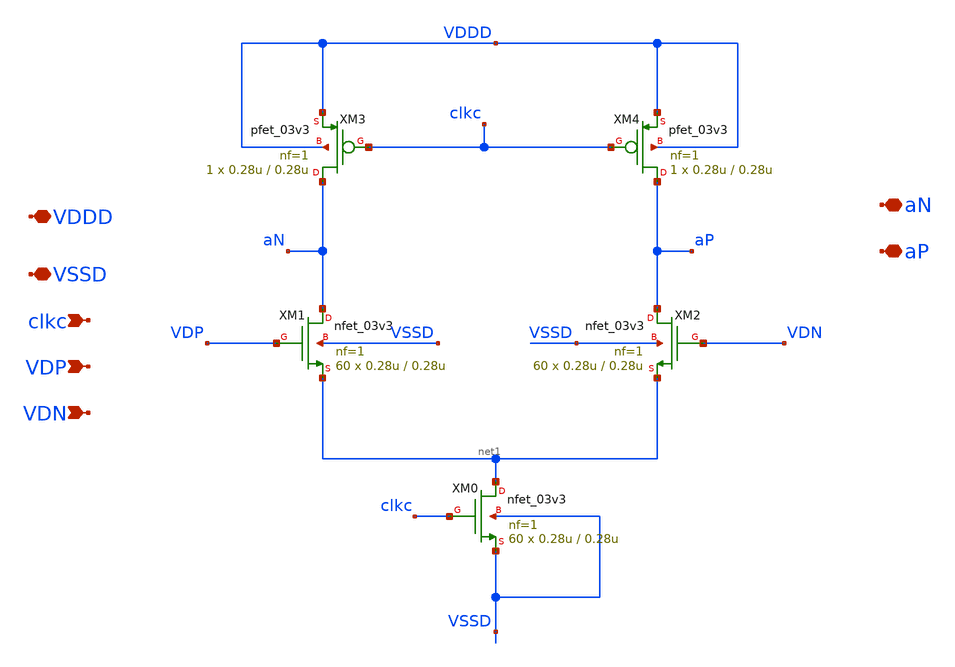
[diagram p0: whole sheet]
** sch_path: SAR_ADC/blocks/Dynamic_Comparator/Dynamic_Comparator_opamp.sch
**.subckt Dynamic_Comparator_opamp VDDD VSSD clkc VDP VDN aN aP
*.iopin VDDD
*.iopin VSSD
*.ipin clkc
*.ipin VDP
*.ipin VDN
*.iopin aN
*.iopin aP
XM0 net1 clkc VSSD VSSD nfet_03v3 L=0.28u W=0.28u nf=1 ad='int((nf+1)/2) * W/nf * 0.18u' as='int((nf+2)/2) * W/nf * 0.18u'
+ pd='2*int((nf+1)/2) * (W/nf + 0.18u)' ps='2*int((nf+2)/2) * (W/nf + 0.18u)' nrd='0.18u / W' nrs='0.18u / W'
+ sa=0 sb=0 sd=0 m=60
XM1 aN VDP net1 VSSD nfet_03v3 L=0.28u W=0.28u nf=1 ad='int((nf+1)/2) * W/nf * 0.18u' as='int((nf+2)/2) * W/nf * 0.18u'
+ pd='2*int((nf+1)/2) * (W/nf + 0.18u)' ps='2*int((nf+2)/2) * (W/nf + 0.18u)' nrd='0.18u / W' nrs='0.18u / W'
+ sa=0 sb=0 sd=0 m=60
XM2 aP VDN net1 VSSD nfet_03v3 L=0.28u W=0.28u nf=1 ad='int((nf+1)/2) * W/nf * 0.18u' as='int((nf+2)/2) * W/nf * 0.18u'
+ pd='2*int((nf+1)/2) * (W/nf + 0.18u)' ps='2*int((nf+2)/2) * (W/nf + 0.18u)' nrd='0.18u / W' nrs='0.18u / W'
+ sa=0 sb=0 sd=0 m=60
XM3 aN clkc VDDD VDDD pfet_03v3 L=0.28u W=0.28u nf=1 ad='int((nf+1)/2) * W/nf * 0.18u' as='int((nf+2)/2) * W/nf * 0.18u'
+ pd='2*int((nf+1)/2) * (W/nf + 0.18u)' ps='2*int((nf+2)/2) * (W/nf + 0.18u)' nrd='0.18u / W' nrs='0.18u / W'
+ sa=0 sb=0 sd=0 m=1
XM4 aP clkc VDDD VDDD pfet_03v3 L=0.28u W=0.28u nf=1 ad='int((nf+1)/2) * W/nf * 0.18u' as='int((nf+2)/2) * W/nf * 0.18u'
+ pd='2*int((nf+1)/2) * (W/nf + 0.18u)' ps='2*int((nf+2)/2) * (W/nf + 0.18u)' nrd='0.18u / W' nrs='0.18u / W'
+ sa=0 sb=0 sd=0 m=1
**.ends
.end
